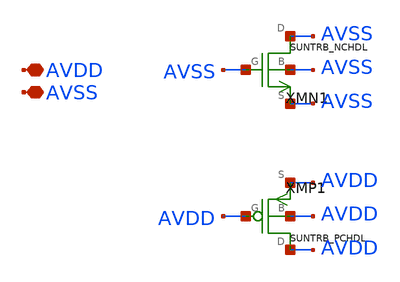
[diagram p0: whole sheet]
** sch_path: ip/sun_trb_sky130nm/design/SUN_TRB_SKY130NM/SUNTRB_TAPCELLB_CV.sch
**.subckt SUNTRB_TAPCELLB_CV AVDD AVSS
*.iopin AVDD
*.iopin AVSS
XMN1 AVSS AVSS AVSS AVSS SUNTRB_NCHDL xoffset=0 yoffset=0 angle=0
XMP1 AVDD AVDD AVDD AVDD SUNTRB_PCHDL xoffset=0 yoffset=0 angle=0
**.ends
.end
